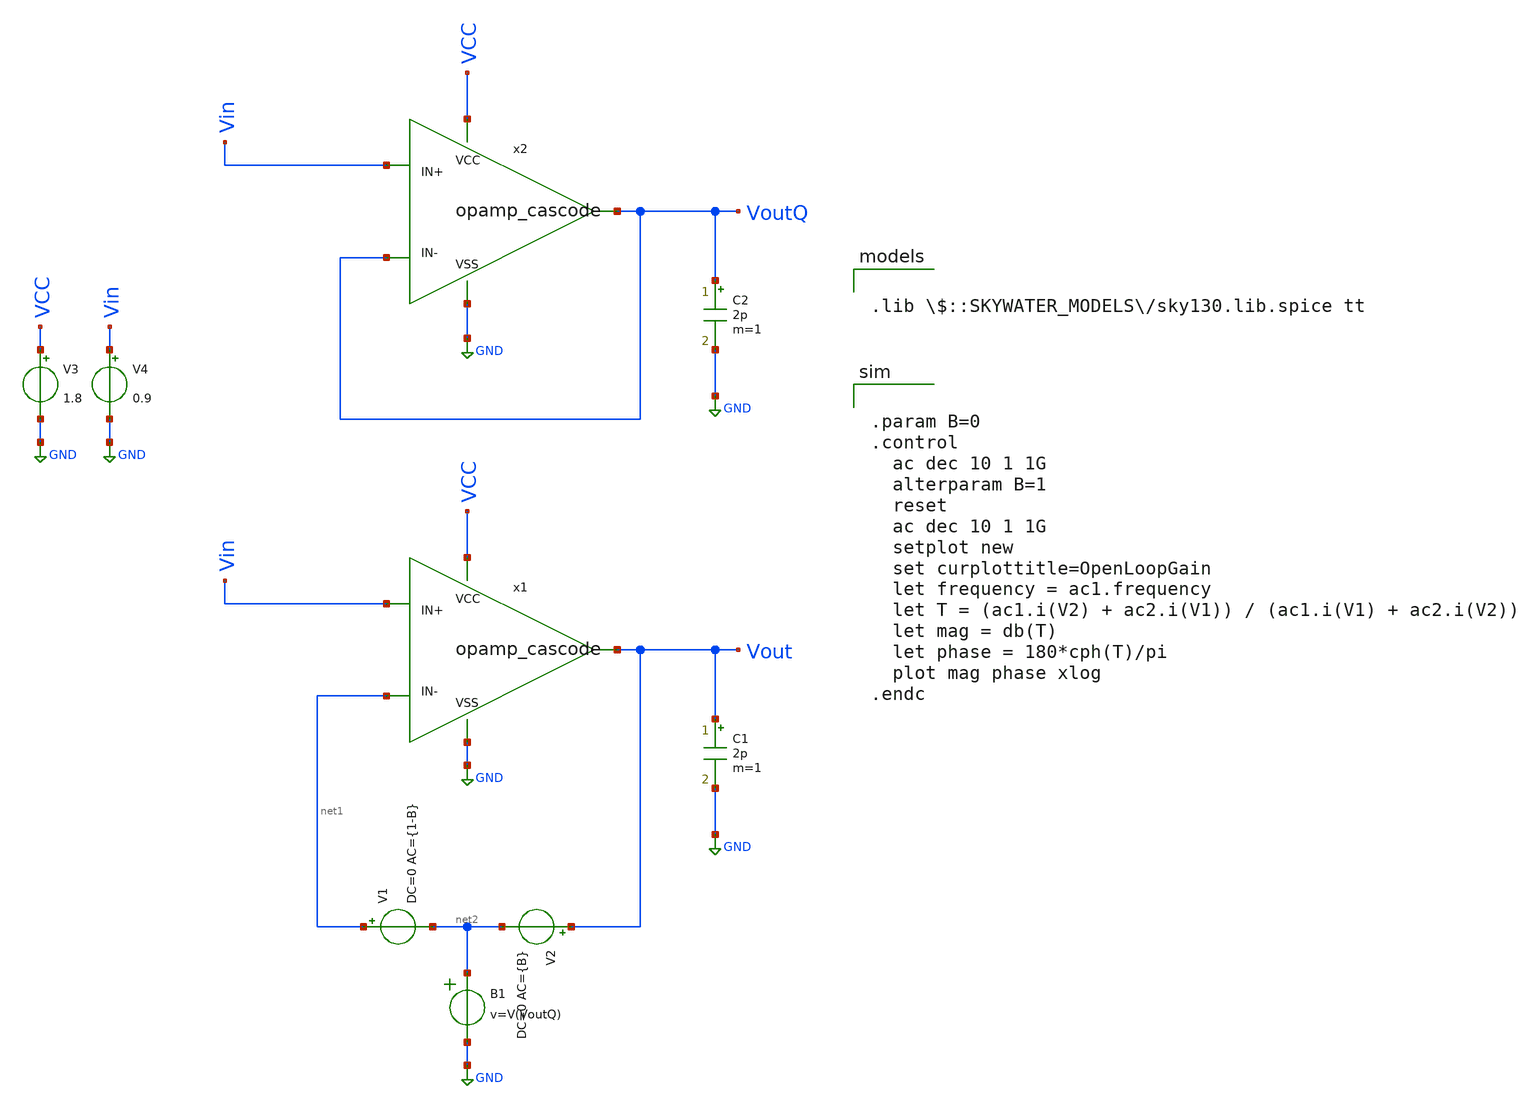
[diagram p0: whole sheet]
** sch_path: opamp_cascode_test_ac.sch
**.subckt opamp_cascode_test_ac
V3 VCC GND 1.8
V4 Vin GND 0.9
V2 Vout net2 DC=0 AC={B}
C1 Vout GND 2p m=1
x1 VCC GND Vin net1 Vout opamp_cascode
x2 VCC GND Vin VoutQ VoutQ opamp_cascode
C2 VoutQ GND 2p m=1
V1 net1 net2 DC=0 AC={1-B}
B1 net2 GND v=V(VoutQ)
**** begin user architecture code


.param B=0
.control
  ac dec 10 1 1G
  alterparam B=1
  reset
  ac dec 10 1 1G
  setplot new
  set curplottitle=OpenLoopGain
  let frequency = ac1.frequency
  let T = (ac1.i(V2) + ac2.i(V1)) / (ac1.i(V1) + ac2.i(V2))
  let mag = db(T)
  let phase = 180*cph(T)/pi
  plot mag phase xlog
.endc



.lib $::SKYWATER_MODELS/sky130.lib.spice tt

**** end user architecture code
**.ends

* expanding   symbol:  /home/zwierzak/projects/Sky130_OpAmp/opamp_cascode.sym # of pins=5
** sym_path: opamp_cascode.sym
** sch_path: opamp_cascode.sch
.subckt opamp_cascode VCC VSS IN+ IN- OUT
*.ipin IN+
*.ipin IN-
*.ipin VCC
*.ipin VSS
*.opin OUT
XM10 net8 net6 VCC VCC sky130_fd_pr__pfet_01v8 L=10 W=40 nf=1 ad='int((nf+1)/2) * W/nf * 0.29' as='int((nf+2)/2) * W/nf * 0.29'
+ pd='2*int((nf+1)/2) * (W/nf + 0.29)' ps='2*int((nf+2)/2) * (W/nf + 0.29)' nrd='0.29 / W' nrs='0.29 / W'
+ sa=0 sb=0 sd=0 mult=2 m=2
XM1 net7 net6 VCC VCC sky130_fd_pr__pfet_01v8 L=10 W=40 nf=1 ad='int((nf+1)/2) * W/nf * 0.29' as='int((nf+2)/2) * W/nf * 0.29'
+ pd='2*int((nf+1)/2) * (W/nf + 0.29)' ps='2*int((nf+2)/2) * (W/nf + 0.29)' nrd='0.29 / W' nrs='0.29 / W'
+ sa=0 sb=0 sd=0 mult=2 m=2
XM5 net3 net9 VCC VCC sky130_fd_pr__pfet_01v8 L=3 W=20 nf=1 ad='int((nf+1)/2) * W/nf * 0.29' as='int((nf+2)/2) * W/nf * 0.29'
+ pd='2*int((nf+1)/2) * (W/nf + 0.29)' ps='2*int((nf+2)/2) * (W/nf + 0.29)' nrd='0.29 / W' nrs='0.29 / W'
+ sa=0 sb=0 sd=0 mult=10 m=10
XM100 net9 net9 VCC VCC sky130_fd_pr__pfet_01v8 L=3 W=20 nf=1 ad='int((nf+1)/2) * W/nf * 0.29' as='int((nf+2)/2) * W/nf * 0.29'
+ pd='2*int((nf+1)/2) * (W/nf + 0.29)' ps='2*int((nf+2)/2) * (W/nf + 0.29)' nrd='0.29 / W' nrs='0.29 / W'
+ sa=0 sb=0 sd=0 mult=1 m=1
I0 net9 VSS 3.5u
XM11 OUT BIAS net8 net8 sky130_fd_pr__pfet_01v8 L=3 W=20 nf=1 ad='int((nf+1)/2) * W/nf * 0.29' as='int((nf+2)/2) * W/nf * 0.29'
+ pd='2*int((nf+1)/2) * (W/nf + 0.29)' ps='2*int((nf+2)/2) * (W/nf + 0.29)' nrd='0.29 / W' nrs='0.29 / W'
+ sa=0 sb=0 sd=0 mult=10 m=10
XM2 net6 BIAS net7 net7 sky130_fd_pr__pfet_01v8 L=3 W=20 nf=1 ad='int((nf+1)/2) * W/nf * 0.29' as='int((nf+2)/2) * W/nf * 0.29'
+ pd='2*int((nf+1)/2) * (W/nf + 0.29)' ps='2*int((nf+2)/2) * (W/nf + 0.29)' nrd='0.29 / W' nrs='0.29 / W'
+ sa=0 sb=0 sd=0 mult=10 m=10
XM6 net1 IN- net3 net3 sky130_fd_pr__pfet_01v8 L=0.25 W=25 nf=2 ad='int((nf+1)/2) * W/nf * 0.29' as='int((nf+2)/2) * W/nf * 0.29'
+ pd='2*int((nf+1)/2) * (W/nf + 0.29)' ps='2*int((nf+2)/2) * (W/nf + 0.29)' nrd='0.29 / W' nrs='0.29 / W'
+ sa=0 sb=0 sd=0 mult=3 m=3
XM8 net2 IN+ net3 net3 sky130_fd_pr__pfet_01v8 L=0.25 W=25 nf=2 ad='int((nf+1)/2) * W/nf * 0.29' as='int((nf+2)/2) * W/nf * 0.29'
+ pd='2*int((nf+1)/2) * (W/nf + 0.29)' ps='2*int((nf+2)/2) * (W/nf + 0.29)' nrd='0.29 / W' nrs='0.29 / W'
+ sa=0 sb=0 sd=0 mult=3 m=3
XM7 net1 net1 VSS VSS sky130_fd_pr__nfet_01v8 L=10 W=20 nf=1 ad='int((nf+1)/2) * W/nf * 0.29' as='int((nf+2)/2) * W/nf * 0.29'
+ pd='2*int((nf+1)/2) * (W/nf + 0.29)' ps='2*int((nf+2)/2) * (W/nf + 0.29)' nrd='0.29 / W' nrs='0.29 / W'
+ sa=0 sb=0 sd=0 mult=1 m=1
XM9 net2 net2 VSS VSS sky130_fd_pr__nfet_01v8 L=10 W=20 nf=1 ad='int((nf+1)/2) * W/nf * 0.29' as='int((nf+2)/2) * W/nf * 0.29'
+ pd='2*int((nf+1)/2) * (W/nf + 0.29)' ps='2*int((nf+2)/2) * (W/nf + 0.29)' nrd='0.29 / W' nrs='0.29 / W'
+ sa=0 sb=0 sd=0 mult=1 m=1
XM13 net4 net2 VSS VSS sky130_fd_pr__nfet_01v8 L=10 W=20 nf=1 ad='int((nf+1)/2) * W/nf * 0.29' as='int((nf+2)/2) * W/nf * 0.29'
+ pd='2*int((nf+1)/2) * (W/nf + 0.29)' ps='2*int((nf+2)/2) * (W/nf + 0.29)' nrd='0.29 / W' nrs='0.29 / W'
+ sa=0 sb=0 sd=0 mult=3 m=3
XM4 net5 net1 VSS VSS sky130_fd_pr__nfet_01v8 L=10 W=20 nf=1 ad='int((nf+1)/2) * W/nf * 0.29' as='int((nf+2)/2) * W/nf * 0.29'
+ pd='2*int((nf+1)/2) * (W/nf + 0.29)' ps='2*int((nf+2)/2) * (W/nf + 0.29)' nrd='0.29 / W' nrs='0.29 / W'
+ sa=0 sb=0 sd=0 mult=3 m=3
XM12 OUT BIAS1 net4 net4 sky130_fd_pr__nfet_01v8 L=3 W=20 nf=1 ad='int((nf+1)/2) * W/nf * 0.29' as='int((nf+2)/2) * W/nf * 0.29'
+ pd='2*int((nf+1)/2) * (W/nf + 0.29)' ps='2*int((nf+2)/2) * (W/nf + 0.29)' nrd='0.29 / W' nrs='0.29 / W'
+ sa=0 sb=0 sd=0 mult=5 m=5
XM3 net6 BIAS1 net5 net5 sky130_fd_pr__nfet_01v8 L=3 W=20 nf=1 ad='int((nf+1)/2) * W/nf * 0.29' as='int((nf+2)/2) * W/nf * 0.29'
+ pd='2*int((nf+1)/2) * (W/nf + 0.29)' ps='2*int((nf+2)/2) * (W/nf + 0.29)' nrd='0.29 / W' nrs='0.29 / W'
+ sa=0 sb=0 sd=0 mult=5 m=5
V1 BIAS VSS 0
V2 BIAS1 VSS 0.6
.ends

.GLOBAL GND
.end
